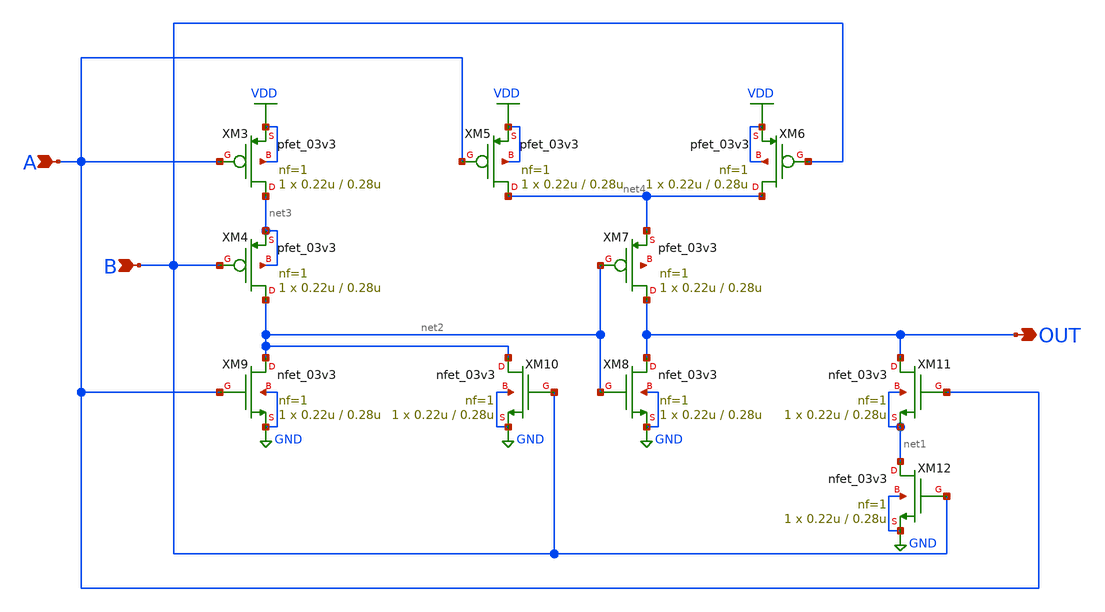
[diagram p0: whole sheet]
** sch_path: Project/1-on-chip/schematic/PNgen/xor.sch
**.subckt xor A OUT B
*.ipin A
*.opin OUT
*.ipin B
XM3 net3 A VDD VDD pfet_03v3 L=0.28u W=0.22u nf=1 ad='int((nf+1)/2) * W/nf * 0.18u' as='int((nf+2)/2) * W/nf * 0.18u'
+ pd='2*int((nf+1)/2) * (W/nf + 0.18u)' ps='2*int((nf+2)/2) * (W/nf + 0.18u)' nrd='0.18u / W' nrs='0.18u / W'
+ sa=0 sb=0 sd=0 m=1
XM4 net2 B net3 net3 pfet_03v3 L=0.28u W=0.22u nf=1 ad='int((nf+1)/2) * W/nf * 0.18u' as='int((nf+2)/2) * W/nf * 0.18u'
+ pd='2*int((nf+1)/2) * (W/nf + 0.18u)' ps='2*int((nf+2)/2) * (W/nf + 0.18u)' nrd='0.18u / W' nrs='0.18u / W'
+ sa=0 sb=0 sd=0 m=1
XM5 net4 A VDD VDD pfet_03v3 L=0.28u W=0.22u nf=1 ad='int((nf+1)/2) * W/nf * 0.18u' as='int((nf+2)/2) * W/nf * 0.18u'
+ pd='2*int((nf+1)/2) * (W/nf + 0.18u)' ps='2*int((nf+2)/2) * (W/nf + 0.18u)' nrd='0.18u / W' nrs='0.18u / W'
+ sa=0 sb=0 sd=0 m=1
XM6 net4 B VDD VDD pfet_03v3 L=0.28u W=0.22u nf=1 ad='int((nf+1)/2) * W/nf * 0.18u' as='int((nf+2)/2) * W/nf * 0.18u'
+ pd='2*int((nf+1)/2) * (W/nf + 0.18u)' ps='2*int((nf+2)/2) * (W/nf + 0.18u)' nrd='0.18u / W' nrs='0.18u / W'
+ sa=0 sb=0 sd=0 m=1
XM7 OUT net2 net4 net5 pfet_03v3 L=0.28u W=0.22u nf=1 ad='int((nf+1)/2) * W/nf * 0.18u' as='int((nf+2)/2) * W/nf * 0.18u'
+ pd='2*int((nf+1)/2) * (W/nf + 0.18u)' ps='2*int((nf+2)/2) * (W/nf + 0.18u)' nrd='0.18u / W' nrs='0.18u / W'
+ sa=0 sb=0 sd=0 m=1
XM8 OUT net2 GND GND nfet_03v3 L=0.28u W=0.22u nf=1 ad='int((nf+1)/2) * W/nf * 0.18u' as='int((nf+2)/2) * W/nf * 0.18u'
+ pd='2*int((nf+1)/2) * (W/nf + 0.18u)' ps='2*int((nf+2)/2) * (W/nf + 0.18u)' nrd='0.18u / W' nrs='0.18u / W'
+ sa=0 sb=0 sd=0 m=1
XM9 net2 A GND GND nfet_03v3 L=0.28u W=0.22u nf=1 ad='int((nf+1)/2) * W/nf * 0.18u' as='int((nf+2)/2) * W/nf * 0.18u'
+ pd='2*int((nf+1)/2) * (W/nf + 0.18u)' ps='2*int((nf+2)/2) * (W/nf + 0.18u)' nrd='0.18u / W' nrs='0.18u / W'
+ sa=0 sb=0 sd=0 m=1
XM10 net2 B GND GND nfet_03v3 L=0.28u W=0.22u nf=1 ad='int((nf+1)/2) * W/nf * 0.18u' as='int((nf+2)/2) * W/nf * 0.18u'
+ pd='2*int((nf+1)/2) * (W/nf + 0.18u)' ps='2*int((nf+2)/2) * (W/nf + 0.18u)' nrd='0.18u / W' nrs='0.18u / W'
+ sa=0 sb=0 sd=0 m=1
XM11 OUT A net1 net1 nfet_03v3 L=0.28u W=0.22u nf=1 ad='int((nf+1)/2) * W/nf * 0.18u' as='int((nf+2)/2) * W/nf * 0.18u'
+ pd='2*int((nf+1)/2) * (W/nf + 0.18u)' ps='2*int((nf+2)/2) * (W/nf + 0.18u)' nrd='0.18u / W' nrs='0.18u / W'
+ sa=0 sb=0 sd=0 m=1
XM12 net1 B GND GND nfet_03v3 L=0.28u W=0.22u nf=1 ad='int((nf+1)/2) * W/nf * 0.18u' as='int((nf+2)/2) * W/nf * 0.18u'
+ pd='2*int((nf+1)/2) * (W/nf + 0.18u)' ps='2*int((nf+2)/2) * (W/nf + 0.18u)' nrd='0.18u / W' nrs='0.18u / W'
+ sa=0 sb=0 sd=0 m=1
**.ends
.GLOBAL VDD
.GLOBAL GND
.end
